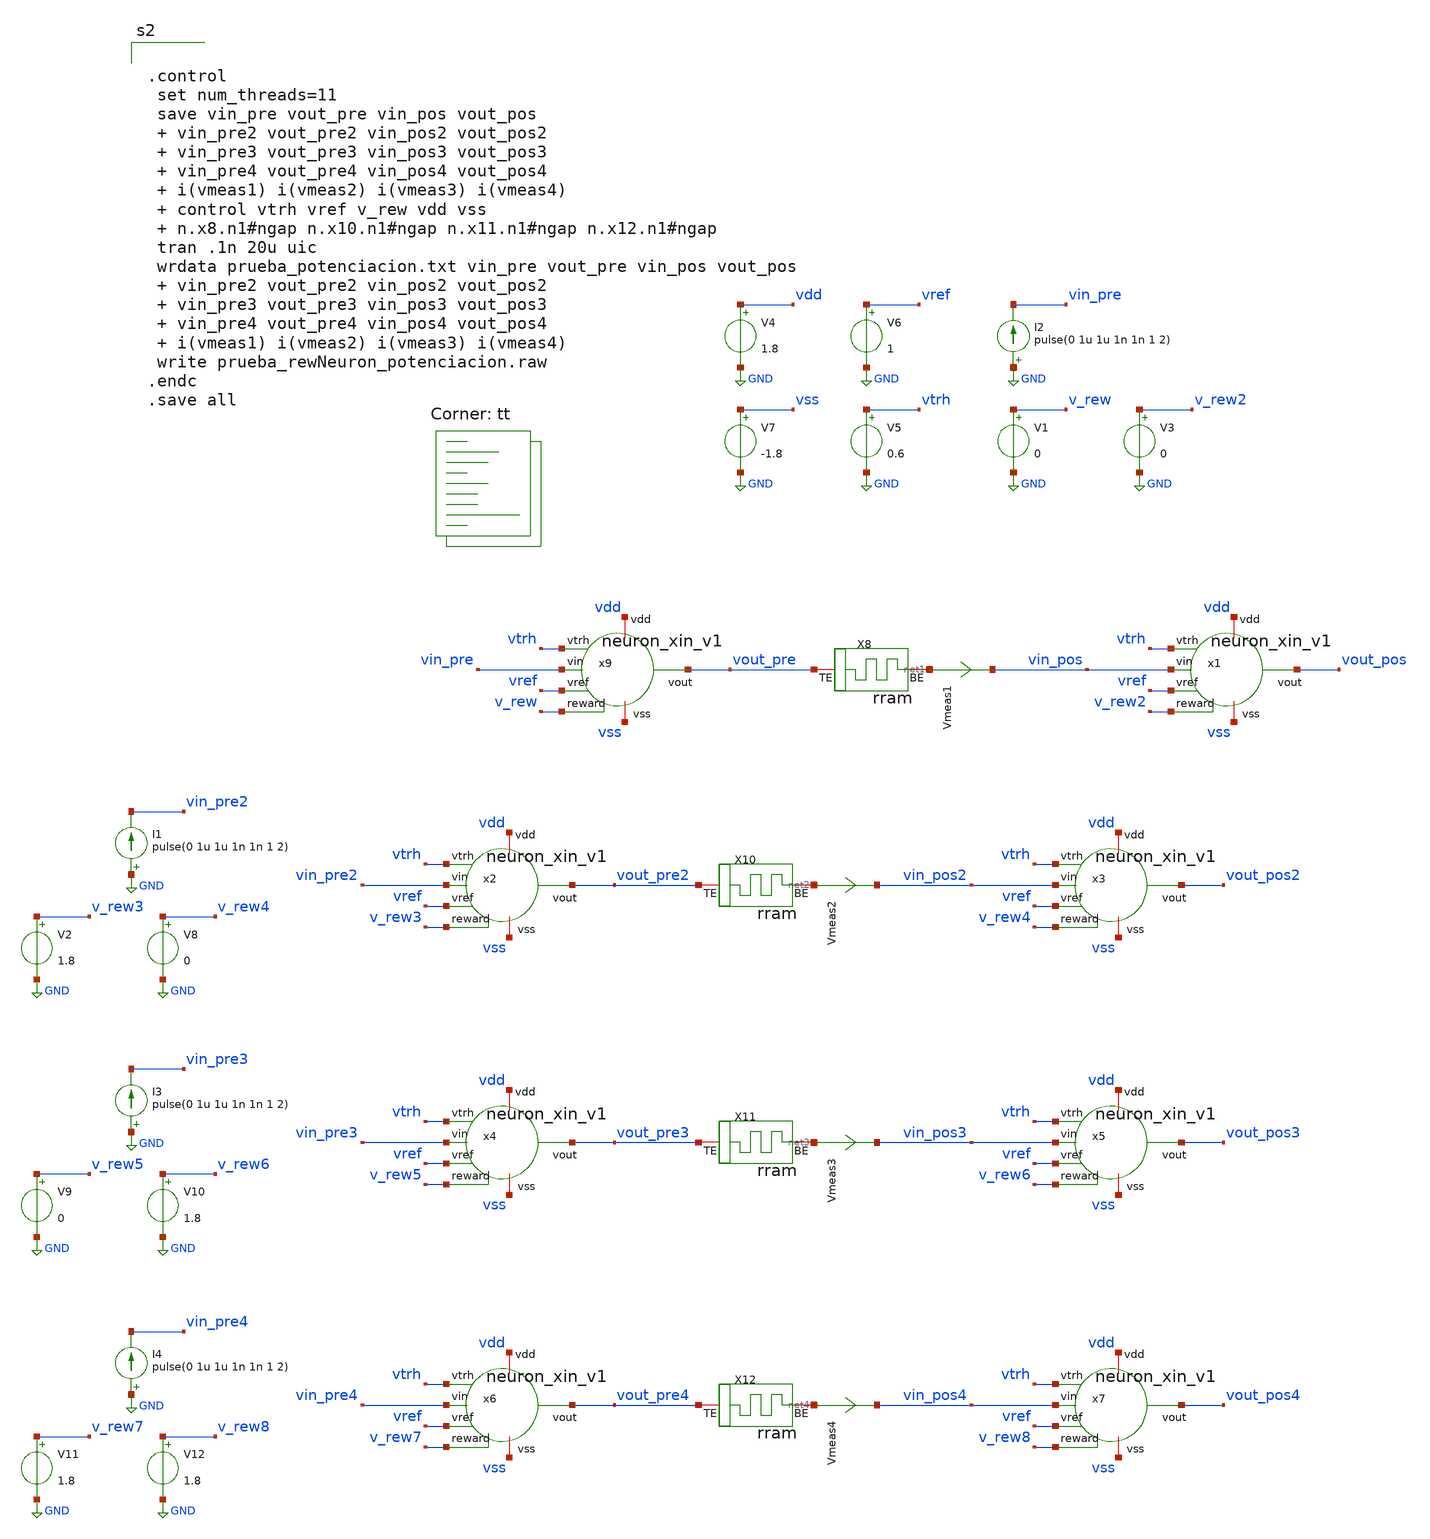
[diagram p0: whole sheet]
** sch_path: designs/tb_xin_neuron_v1/prueba_rewNeuron_potenciacion.sch
**.subckt prueba_rewNeuron_potenciacion
V4 vdd GND 1.8
V5 vtrh GND 0.6
V6 vref GND 1
V7 vss GND -1.8
V1 v_rew GND 0
Vmeas1 net1 vin_pos 0
.save i(vmeas1)
I2 GND vin_pre pulse(0 1u 1u 1n 1n 1 2)
Vmeas2 net2 vin_pos2 0
.save i(vmeas2)
V2 v_rew3 GND 1.8
I1 GND vin_pre2 pulse(0 1u 1u 1n 1n 1 2)
V3 v_rew2 GND 0
V8 v_rew4 GND 0
Vmeas3 net3 vin_pos3 0
.save i(vmeas3)
V9 v_rew5 GND 0
I3 GND vin_pre3 pulse(0 1u 1u 1n 1n 1 2)
V10 v_rew6 GND 1.8
Vmeas4 net4 vin_pos4 0
.save i(vmeas4)
V11 v_rew7 GND 1.8
I4 GND vin_pre4 pulse(0 1u 1u 1n 1n 1 2)
V12 v_rew8 GND 1.8
x9 vdd vss vout_pre vin_pre vtrh vref v_rew neuron_xin_v1
x1 vdd vss vout_pos vin_pos vtrh vref v_rew2 neuron_xin_v1
x2 vdd vss vout_pre2 vin_pre2 vtrh vref v_rew3 neuron_xin_v1
x3 vdd vss vout_pos2 vin_pos2 vtrh vref v_rew4 neuron_xin_v1
x4 vdd vss vout_pre3 vin_pre3 vtrh vref v_rew5 neuron_xin_v1
x5 vdd vss vout_pos3 vin_pos3 vtrh vref v_rew6 neuron_xin_v1
x6 vdd vss vout_pre4 vin_pre4 vtrh vref v_rew7 neuron_xin_v1
x7 vdd vss vout_pos4 vin_pos4 vtrh vref v_rew8 neuron_xin_v1
X8 vout_pre net1 rram_cell
X10 vout_pre2 net2 rram_cell
X11 vout_pre3 net3 rram_cell
X12 vout_pre4 net4 rram_cell
**** begin user architecture code


.control
 set num_threads=11
 save vin_pre vout_pre vin_pos vout_pos
 + vin_pre2 vout_pre2 vin_pos2 vout_pos2
 + vin_pre3 vout_pre3 vin_pos3 vout_pos3
 + vin_pre4 vout_pre4 vin_pos4 vout_pos4
 + i(vmeas1) i(vmeas2) i(vmeas3) i(vmeas4)
 + control vtrh vref v_rew vdd vss
 + n.x8.n1#ngap n.x10.n1#ngap n.x11.n1#ngap n.x12.n1#ngap
 tran .1n 20u uic
 wrdata prueba_potenciacion.txt vin_pre vout_pre vin_pos vout_pos
 + vin_pre2 vout_pre2 vin_pos2 vout_pos2
 + vin_pre3 vout_pre3 vin_pos3 vout_pos3
 + vin_pre4 vout_pre4 vin_pos4 vout_pos4
 + i(vmeas1) i(vmeas2) i(vmeas3) i(vmeas4)
 write prueba_rewNeuron_potenciacion.raw
.endc
.save all


.lib $::SKYWATER_MODELS/sky130.lib.spice tt

.subckt rram_cell BE TE
N1 BE TE rram_model
.ends rram_cell

.model rram_model rram gap_initial=0.85
*0.1-1.7

.control
pre_osdi /foss/designs/spike_130/designs/memristors/rram_v1/rram.osdi
.endc

**** end user architecture code
**.ends
.GLOBAL GND
.end
